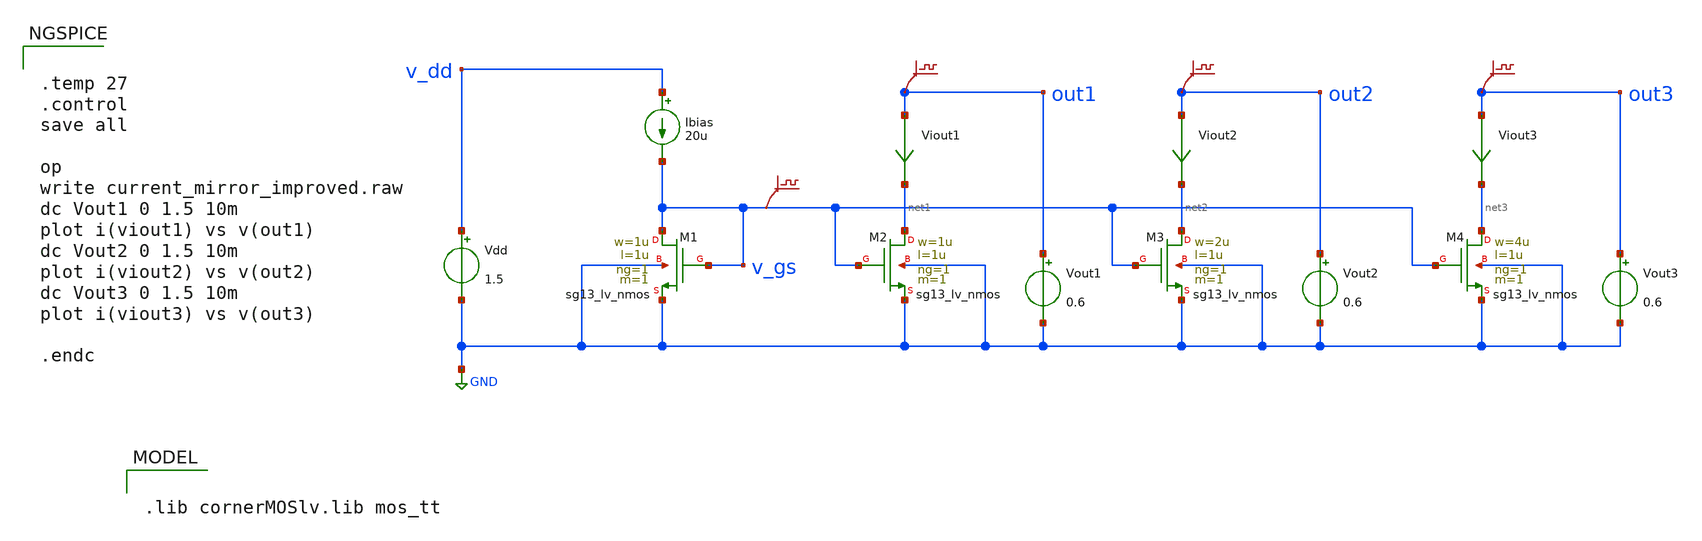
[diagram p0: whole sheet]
** sch_path: Modulo_Analogico/Lab4/current_mirror_improved.sch
**.subckt current_mirror_improved
Vdd v_dd GND 1.5
Ibias v_dd v_gs 20u
Vout1 out1 GND 0.6
Vout2 out2 GND 0.6
Vout3 out3 GND 0.6
.save v(out1)
.save v(out2)
.save v(out3)
.save v(v_gs)
Viout1 out1 net1 0
.save i(viout1)
Viout2 out2 net2 0
.save i(viout2)
Viout3 out3 net3 0
.save i(viout3)
XM1 v_gs v_gs GND GND sg13_lv_nmos w=1u l=1u ng=1 m=1 mm_ok=1
XM2 net1 v_gs GND GND sg13_lv_nmos w=1u l=1u ng=1 m=1 mm_ok=1
XM3 net2 v_gs GND GND sg13_lv_nmos w=2u l=1u ng=1 m=1 mm_ok=1
XM4 net3 v_gs GND GND sg13_lv_nmos w=4u l=1u ng=1 m=1 mm_ok=1
**** begin user architecture code


.temp 27
.control
save all

op
write current_mirror_improved.raw
dc Vout1 0 1.5 10m
plot i(viout1) vs v(out1)
dc Vout2 0 1.5 10m
plot i(viout2) vs v(out2)
dc Vout3 0 1.5 10m
plot i(viout3) vs v(out3)

.endc



.lib cornerMOSlv.lib mos_tt

**** end user architecture code
**.ends
.GLOBAL GND
.end
